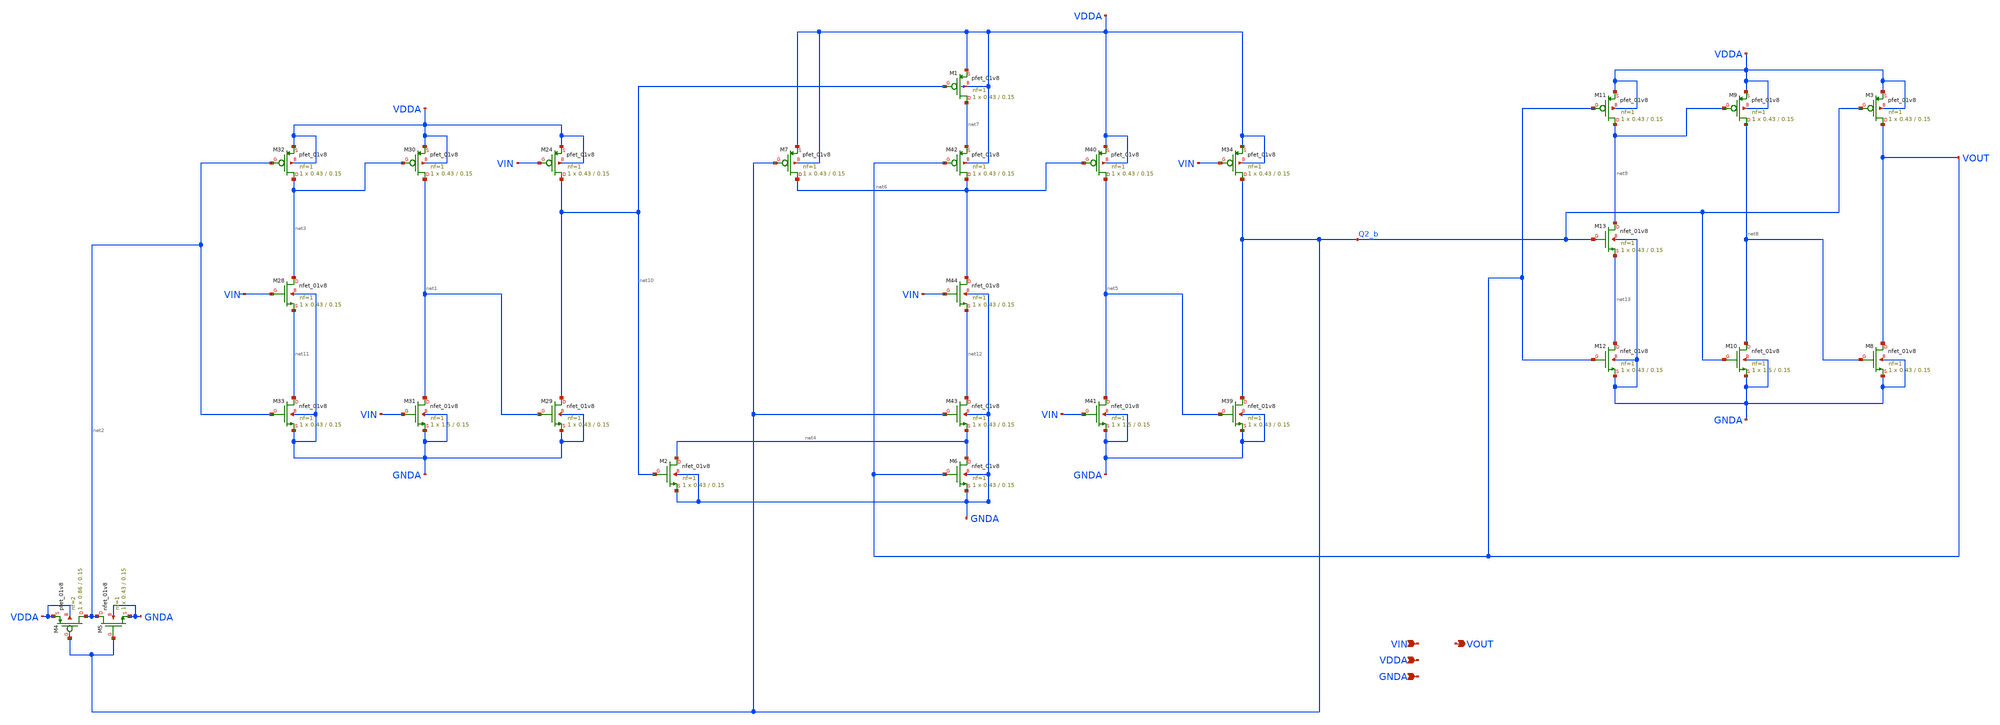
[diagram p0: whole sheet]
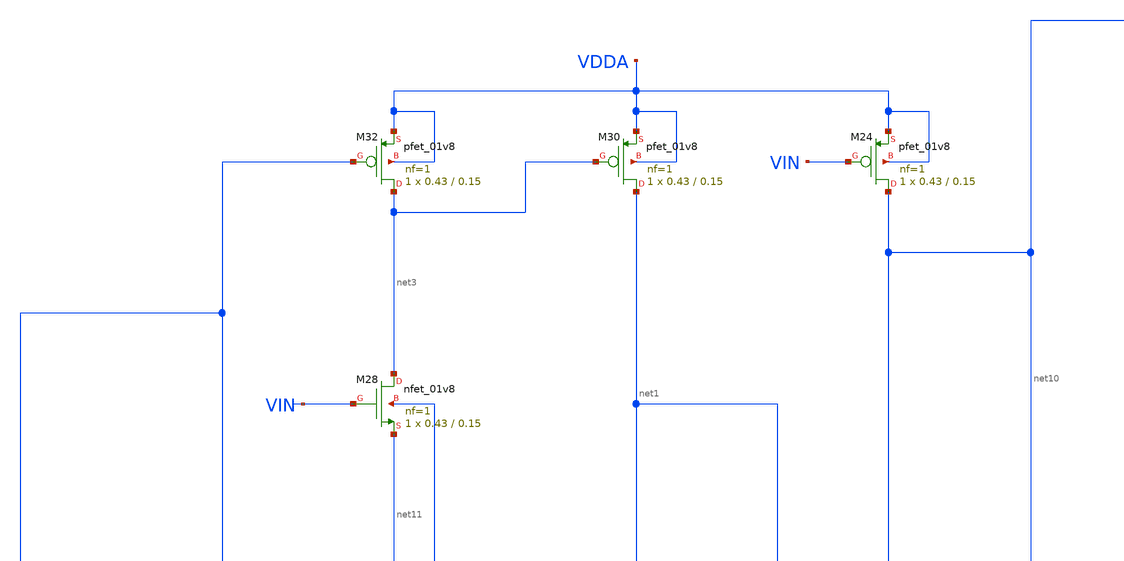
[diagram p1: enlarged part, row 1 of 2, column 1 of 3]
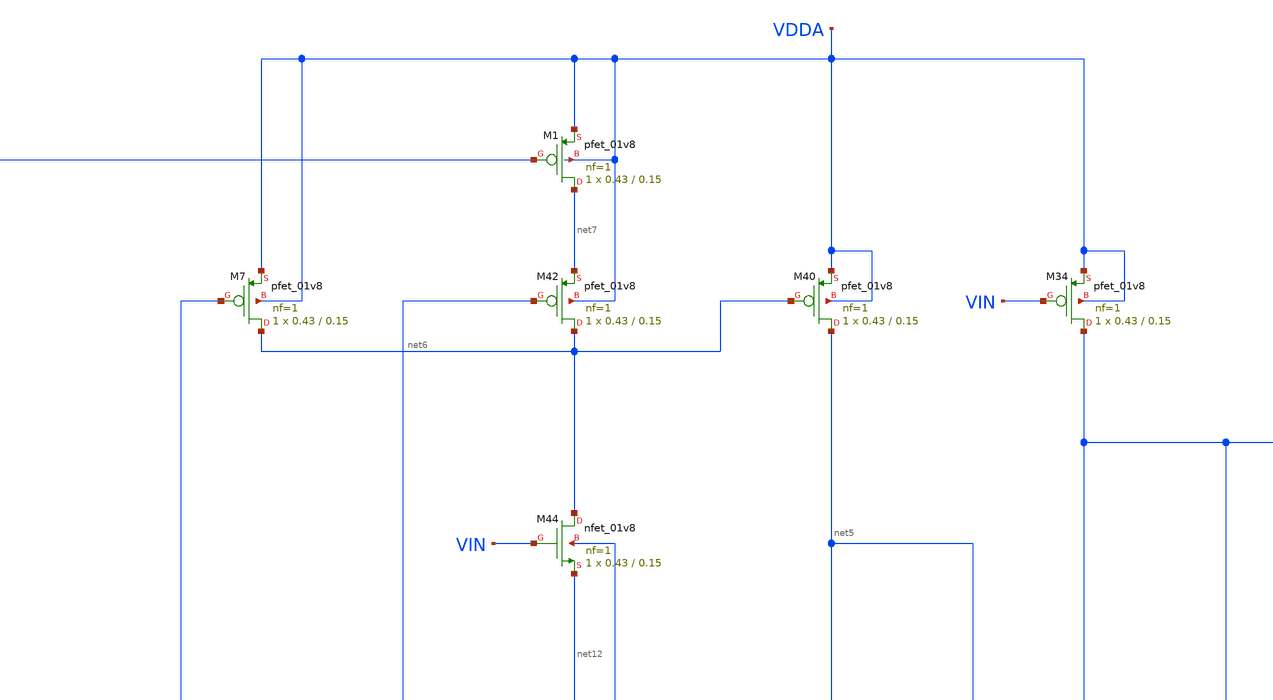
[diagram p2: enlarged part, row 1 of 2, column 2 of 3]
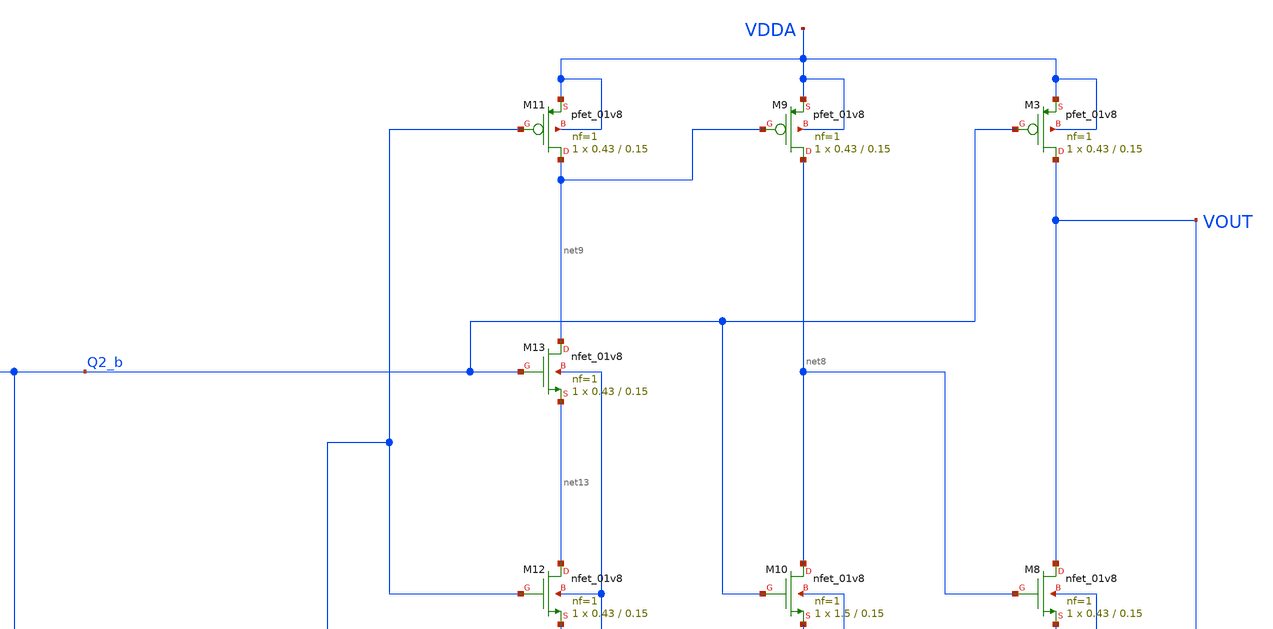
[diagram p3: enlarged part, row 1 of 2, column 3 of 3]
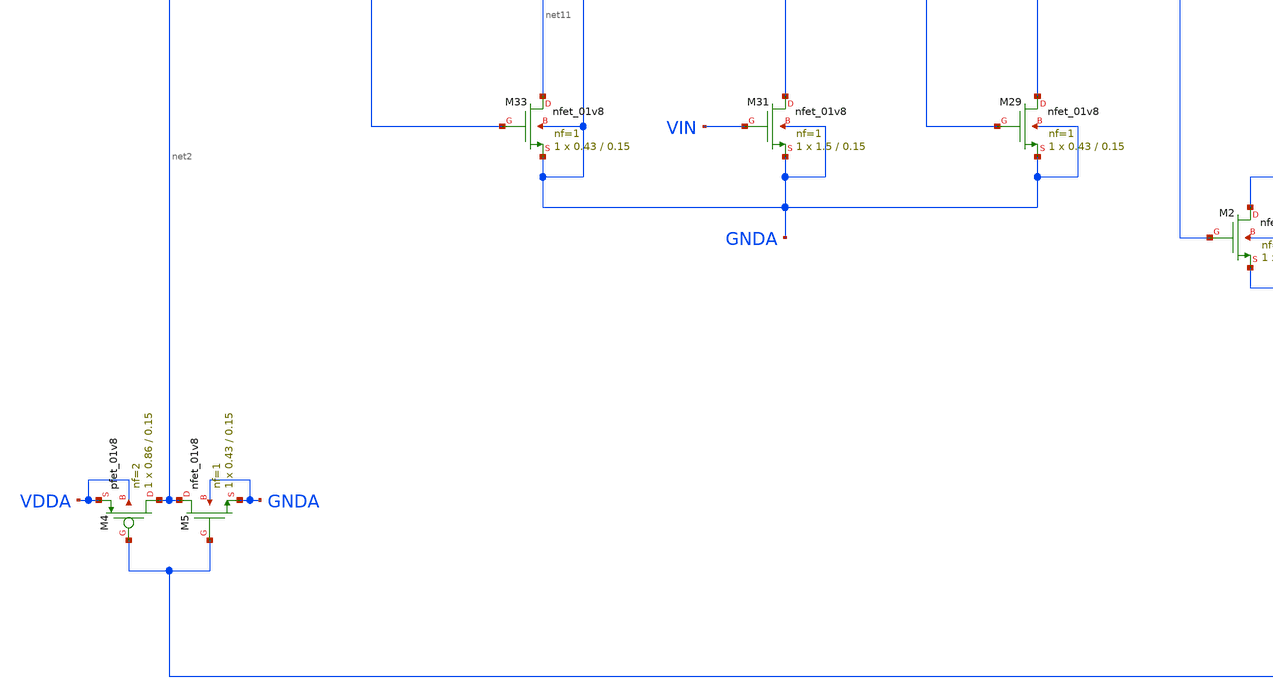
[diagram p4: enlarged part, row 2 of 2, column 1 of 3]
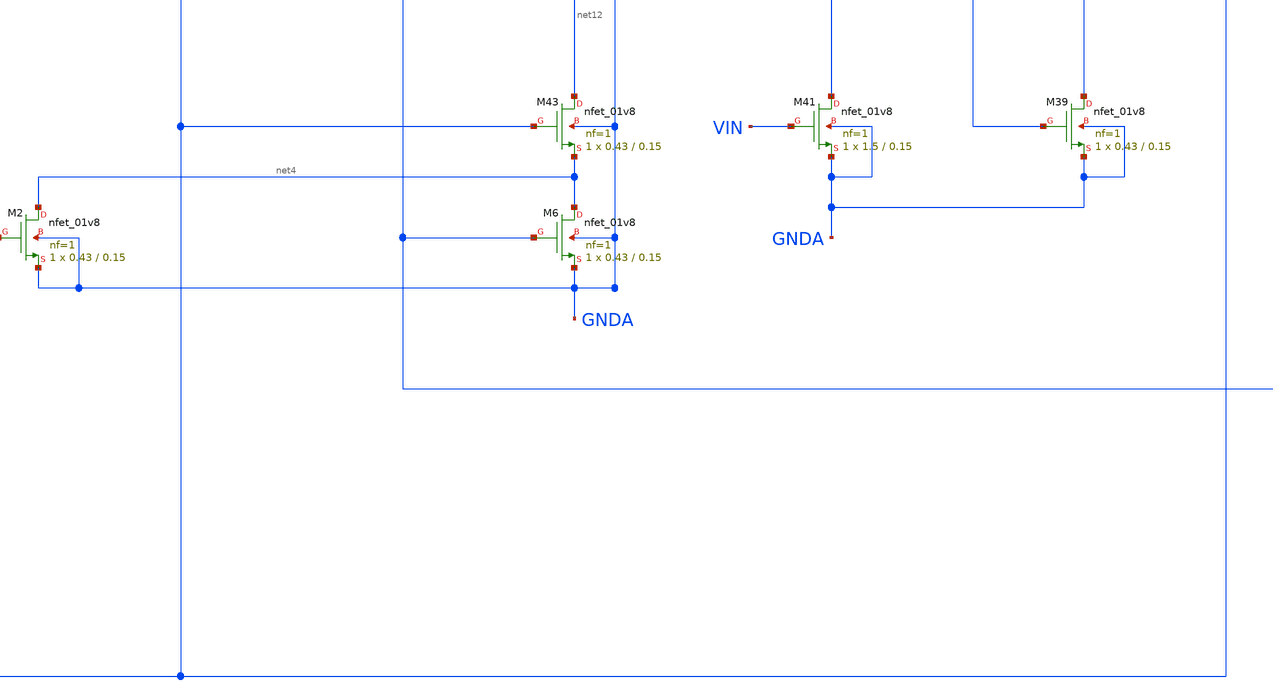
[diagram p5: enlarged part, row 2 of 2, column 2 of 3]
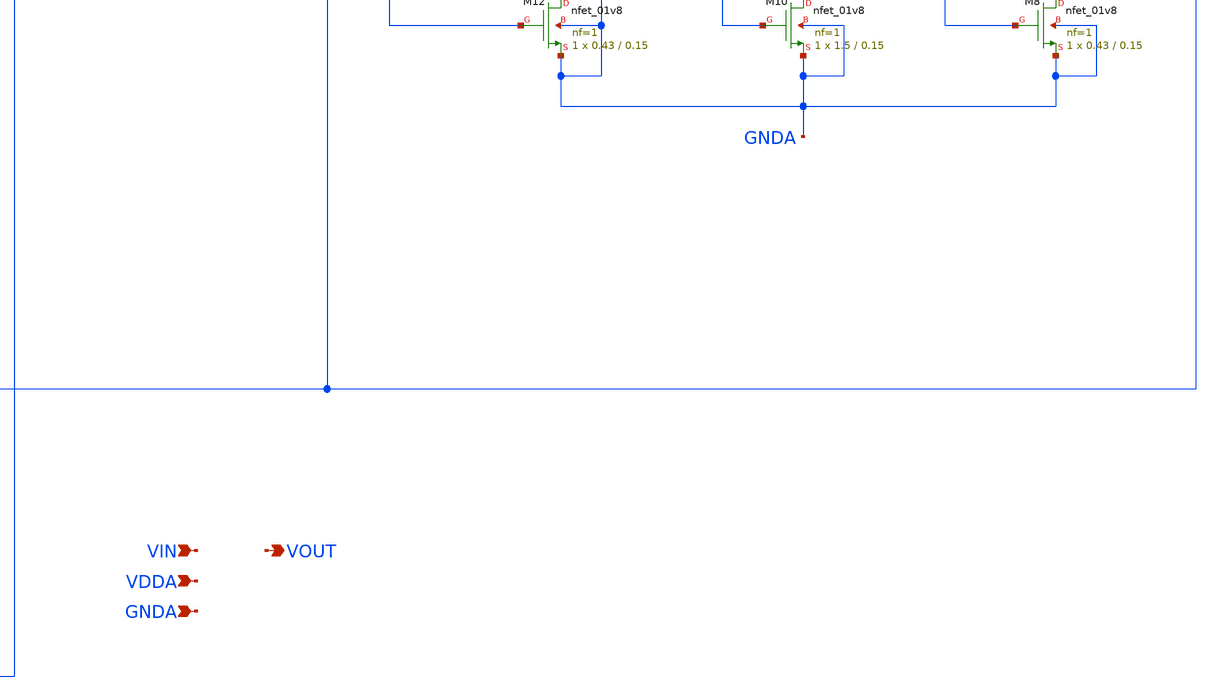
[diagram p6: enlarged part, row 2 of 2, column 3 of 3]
** sch_path: projects/pll/divider/xschem_ngspice/TSPC_FF_ratioed_divide5_2.sch
**.subckt TSPC_FF_ratioed_divide5_2 VIN VOUT VDDA GNDA
*.ipin VIN
*.opin VOUT
*.ipin VDDA
*.ipin GNDA
XM24 net10 VIN VDDA VDDA sky130_fd_pr__pfet_01v8 L=0.15 W=0.43 nf=1 ad='int((nf+1)/2) * W/nf * 0.29'
+ as='int((nf+2)/2) * W/nf * 0.29' pd='2*int((nf+1)/2) * (W/nf + 0.29)' ps='2*int((nf+2)/2) * (W/nf + 0.29)'
+ nrd='0.29 / W' nrs='0.29 / W' sa=0 sb=0 sd=0 mult=1 m=1
XM29 net10 net1 GNDA GNDA sky130_fd_pr__nfet_01v8 L=0.15 W=0.43 nf=1 ad='int((nf+1)/2) * W/nf * 0.29'
+ as='int((nf+2)/2) * W/nf * 0.29' pd='2*int((nf+1)/2) * (W/nf + 0.29)' ps='2*int((nf+2)/2) * (W/nf + 0.29)'
+ nrd='0.29 / W' nrs='0.29 / W' sa=0 sb=0 sd=0 mult=1 m=1
XM30 net1 net3 VDDA VDDA sky130_fd_pr__pfet_01v8 L=0.15 W=0.43 nf=1 ad='int((nf+1)/2) * W/nf * 0.29'
+ as='int((nf+2)/2) * W/nf * 0.29' pd='2*int((nf+1)/2) * (W/nf + 0.29)' ps='2*int((nf+2)/2) * (W/nf + 0.29)'
+ nrd='0.29 / W' nrs='0.29 / W' sa=0 sb=0 sd=0 mult=1 m=1
XM31 net1 VIN GNDA GNDA sky130_fd_pr__nfet_01v8 L=0.15 W=1.5 nf=1 ad='int((nf+1)/2) * W/nf * 0.29' as='int((nf+2)/2) * W/nf * 0.29'
+ pd='2*int((nf+1)/2) * (W/nf + 0.29)' ps='2*int((nf+2)/2) * (W/nf + 0.29)' nrd='0.29 / W' nrs='0.29 / W'
+ sa=0 sb=0 sd=0 mult=1 m=1
XM32 net3 net2 VDDA VDDA sky130_fd_pr__pfet_01v8 L=0.15 W=0.43 nf=1 ad='int((nf+1)/2) * W/nf * 0.29'
+ as='int((nf+2)/2) * W/nf * 0.29' pd='2*int((nf+1)/2) * (W/nf + 0.29)' ps='2*int((nf+2)/2) * (W/nf + 0.29)'
+ nrd='0.29 / W' nrs='0.29 / W' sa=0 sb=0 sd=0 mult=1 m=1
XM33 net11 net2 GNDA GNDA sky130_fd_pr__nfet_01v8 L=0.15 W=0.43 nf=1 ad='int((nf+1)/2) * W/nf * 0.29'
+ as='int((nf+2)/2) * W/nf * 0.29' pd='2*int((nf+1)/2) * (W/nf + 0.29)' ps='2*int((nf+2)/2) * (W/nf + 0.29)'
+ nrd='0.29 / W' nrs='0.29 / W' sa=0 sb=0 sd=0 mult=1 m=1
XM28 net3 VIN net11 GNDA sky130_fd_pr__nfet_01v8 L=0.15 W=0.43 nf=1 ad='int((nf+1)/2) * W/nf * 0.29'
+ as='int((nf+2)/2) * W/nf * 0.29' pd='2*int((nf+1)/2) * (W/nf + 0.29)' ps='2*int((nf+2)/2) * (W/nf + 0.29)'
+ nrd='0.29 / W' nrs='0.29 / W' sa=0 sb=0 sd=0 mult=1 m=1
XM34 Q2_b VIN VDDA VDDA sky130_fd_pr__pfet_01v8 L=0.15 W=0.43 nf=1 ad='int((nf+1)/2) * W/nf * 0.29' as='int((nf+2)/2) * W/nf * 0.29'
+ pd='2*int((nf+1)/2) * (W/nf + 0.29)' ps='2*int((nf+2)/2) * (W/nf + 0.29)' nrd='0.29 / W' nrs='0.29 / W'
+ sa=0 sb=0 sd=0 mult=1 m=1
XM39 Q2_b net5 GNDA GNDA sky130_fd_pr__nfet_01v8 L=0.15 W=0.43 nf=1 ad='int((nf+1)/2) * W/nf * 0.29'
+ as='int((nf+2)/2) * W/nf * 0.29' pd='2*int((nf+1)/2) * (W/nf + 0.29)' ps='2*int((nf+2)/2) * (W/nf + 0.29)'
+ nrd='0.29 / W' nrs='0.29 / W' sa=0 sb=0 sd=0 mult=1 m=1
XM40 net5 net6 VDDA VDDA sky130_fd_pr__pfet_01v8 L=0.15 W=0.43 nf=1 ad='int((nf+1)/2) * W/nf * 0.29'
+ as='int((nf+2)/2) * W/nf * 0.29' pd='2*int((nf+1)/2) * (W/nf + 0.29)' ps='2*int((nf+2)/2) * (W/nf + 0.29)'
+ nrd='0.29 / W' nrs='0.29 / W' sa=0 sb=0 sd=0 mult=1 m=1
XM41 net5 VIN GNDA GNDA sky130_fd_pr__nfet_01v8 L=0.15 W=1.5 nf=1 ad='int((nf+1)/2) * W/nf * 0.29' as='int((nf+2)/2) * W/nf * 0.29'
+ pd='2*int((nf+1)/2) * (W/nf + 0.29)' ps='2*int((nf+2)/2) * (W/nf + 0.29)' nrd='0.29 / W' nrs='0.29 / W'
+ sa=0 sb=0 sd=0 mult=1 m=1
XM42 net6 VOUT net7 VDDA sky130_fd_pr__pfet_01v8 L=0.15 W=0.43 nf=1 ad='int((nf+1)/2) * W/nf * 0.29'
+ as='int((nf+2)/2) * W/nf * 0.29' pd='2*int((nf+1)/2) * (W/nf + 0.29)' ps='2*int((nf+2)/2) * (W/nf + 0.29)'
+ nrd='0.29 / W' nrs='0.29 / W' sa=0 sb=0 sd=0 mult=1 m=1
XM43 net12 Q2_b net4 GNDA sky130_fd_pr__nfet_01v8 L=0.15 W=0.43 nf=1 ad='int((nf+1)/2) * W/nf * 0.29'
+ as='int((nf+2)/2) * W/nf * 0.29' pd='2*int((nf+1)/2) * (W/nf + 0.29)' ps='2*int((nf+2)/2) * (W/nf + 0.29)'
+ nrd='0.29 / W' nrs='0.29 / W' sa=0 sb=0 sd=0 mult=1 m=1
XM44 net6 VIN net12 GNDA sky130_fd_pr__nfet_01v8 L=0.15 W=0.43 nf=1 ad='int((nf+1)/2) * W/nf * 0.29'
+ as='int((nf+2)/2) * W/nf * 0.29' pd='2*int((nf+1)/2) * (W/nf + 0.29)' ps='2*int((nf+2)/2) * (W/nf + 0.29)'
+ nrd='0.29 / W' nrs='0.29 / W' sa=0 sb=0 sd=0 mult=1 m=1
XM4 net2 Q2_b VDDA VDDA sky130_fd_pr__pfet_01v8 L=0.15 W=0.86 nf=2 ad='int((nf+1)/2) * W/nf * 0.29' as='int((nf+2)/2) * W/nf * 0.29'
+ pd='2*int((nf+1)/2) * (W/nf + 0.29)' ps='2*int((nf+2)/2) * (W/nf + 0.29)' nrd='0.29 / W' nrs='0.29 / W'
+ sa=0 sb=0 sd=0 mult=1 m=1
XM5 net2 Q2_b GNDA GNDA sky130_fd_pr__nfet_01v8 L=0.15 W=0.43 nf=1 ad='int((nf+1)/2) * W/nf * 0.29' as='int((nf+2)/2) * W/nf * 0.29'
+ pd='2*int((nf+1)/2) * (W/nf + 0.29)' ps='2*int((nf+2)/2) * (W/nf + 0.29)' nrd='0.29 / W' nrs='0.29 / W'
+ sa=0 sb=0 sd=0 mult=1 m=1
XM6 net4 VOUT GNDA GNDA sky130_fd_pr__nfet_01v8 L=0.15 W=0.43 nf=1 ad='int((nf+1)/2) * W/nf * 0.29' as='int((nf+2)/2) * W/nf * 0.29'
+ pd='2*int((nf+1)/2) * (W/nf + 0.29)' ps='2*int((nf+2)/2) * (W/nf + 0.29)' nrd='0.29 / W' nrs='0.29 / W'
+ sa=0 sb=0 sd=0 mult=1 m=1
XM7 net6 Q2_b VDDA VDDA sky130_fd_pr__pfet_01v8 L=0.15 W=0.43 nf=1 ad='int((nf+1)/2) * W/nf * 0.29' as='int((nf+2)/2) * W/nf * 0.29'
+ pd='2*int((nf+1)/2) * (W/nf + 0.29)' ps='2*int((nf+2)/2) * (W/nf + 0.29)' nrd='0.29 / W' nrs='0.29 / W'
+ sa=0 sb=0 sd=0 mult=1 m=1
XM1 net7 net10 VDDA VDDA sky130_fd_pr__pfet_01v8 L=0.15 W=0.43 nf=1 ad='int((nf+1)/2) * W/nf * 0.29'
+ as='int((nf+2)/2) * W/nf * 0.29' pd='2*int((nf+1)/2) * (W/nf + 0.29)' ps='2*int((nf+2)/2) * (W/nf + 0.29)'
+ nrd='0.29 / W' nrs='0.29 / W' sa=0 sb=0 sd=0 mult=1 m=1
XM2 net4 net10 GNDA GNDA sky130_fd_pr__nfet_01v8 L=0.15 W=0.43 nf=1 ad='int((nf+1)/2) * W/nf * 0.29'
+ as='int((nf+2)/2) * W/nf * 0.29' pd='2*int((nf+1)/2) * (W/nf + 0.29)' ps='2*int((nf+2)/2) * (W/nf + 0.29)'
+ nrd='0.29 / W' nrs='0.29 / W' sa=0 sb=0 sd=0 mult=1 m=1
XM3 VOUT Q2_b VDDA VDDA sky130_fd_pr__pfet_01v8 L=0.15 W=0.43 nf=1 ad='int((nf+1)/2) * W/nf * 0.29' as='int((nf+2)/2) * W/nf * 0.29'
+ pd='2*int((nf+1)/2) * (W/nf + 0.29)' ps='2*int((nf+2)/2) * (W/nf + 0.29)' nrd='0.29 / W' nrs='0.29 / W'
+ sa=0 sb=0 sd=0 mult=1 m=1
XM8 VOUT net8 GNDA GNDA sky130_fd_pr__nfet_01v8 L=0.15 W=0.43 nf=1 ad='int((nf+1)/2) * W/nf * 0.29' as='int((nf+2)/2) * W/nf * 0.29'
+ pd='2*int((nf+1)/2) * (W/nf + 0.29)' ps='2*int((nf+2)/2) * (W/nf + 0.29)' nrd='0.29 / W' nrs='0.29 / W'
+ sa=0 sb=0 sd=0 mult=1 m=1
XM9 net8 net9 VDDA VDDA sky130_fd_pr__pfet_01v8 L=0.15 W=0.43 nf=1 ad='int((nf+1)/2) * W/nf * 0.29' as='int((nf+2)/2) * W/nf * 0.29'
+ pd='2*int((nf+1)/2) * (W/nf + 0.29)' ps='2*int((nf+2)/2) * (W/nf + 0.29)' nrd='0.29 / W' nrs='0.29 / W'
+ sa=0 sb=0 sd=0 mult=1 m=1
XM10 net8 Q2_b GNDA GNDA sky130_fd_pr__nfet_01v8 L=0.15 W=1.5 nf=1 ad='int((nf+1)/2) * W/nf * 0.29' as='int((nf+2)/2) * W/nf * 0.29'
+ pd='2*int((nf+1)/2) * (W/nf + 0.29)' ps='2*int((nf+2)/2) * (W/nf + 0.29)' nrd='0.29 / W' nrs='0.29 / W'
+ sa=0 sb=0 sd=0 mult=1 m=1
XM11 net9 VOUT VDDA VDDA sky130_fd_pr__pfet_01v8 L=0.15 W=0.43 nf=1 ad='int((nf+1)/2) * W/nf * 0.29'
+ as='int((nf+2)/2) * W/nf * 0.29' pd='2*int((nf+1)/2) * (W/nf + 0.29)' ps='2*int((nf+2)/2) * (W/nf + 0.29)'
+ nrd='0.29 / W' nrs='0.29 / W' sa=0 sb=0 sd=0 mult=1 m=1
XM12 net13 VOUT GNDA GNDA sky130_fd_pr__nfet_01v8 L=0.15 W=0.43 nf=1 ad='int((nf+1)/2) * W/nf * 0.29'
+ as='int((nf+2)/2) * W/nf * 0.29' pd='2*int((nf+1)/2) * (W/nf + 0.29)' ps='2*int((nf+2)/2) * (W/nf + 0.29)'
+ nrd='0.29 / W' nrs='0.29 / W' sa=0 sb=0 sd=0 mult=1 m=1
XM13 net9 Q2_b net13 GNDA sky130_fd_pr__nfet_01v8 L=0.15 W=0.43 nf=1 ad='int((nf+1)/2) * W/nf * 0.29'
+ as='int((nf+2)/2) * W/nf * 0.29' pd='2*int((nf+1)/2) * (W/nf + 0.29)' ps='2*int((nf+2)/2) * (W/nf + 0.29)'
+ nrd='0.29 / W' nrs='0.29 / W' sa=0 sb=0 sd=0 mult=1 m=1
**.ends
.end
